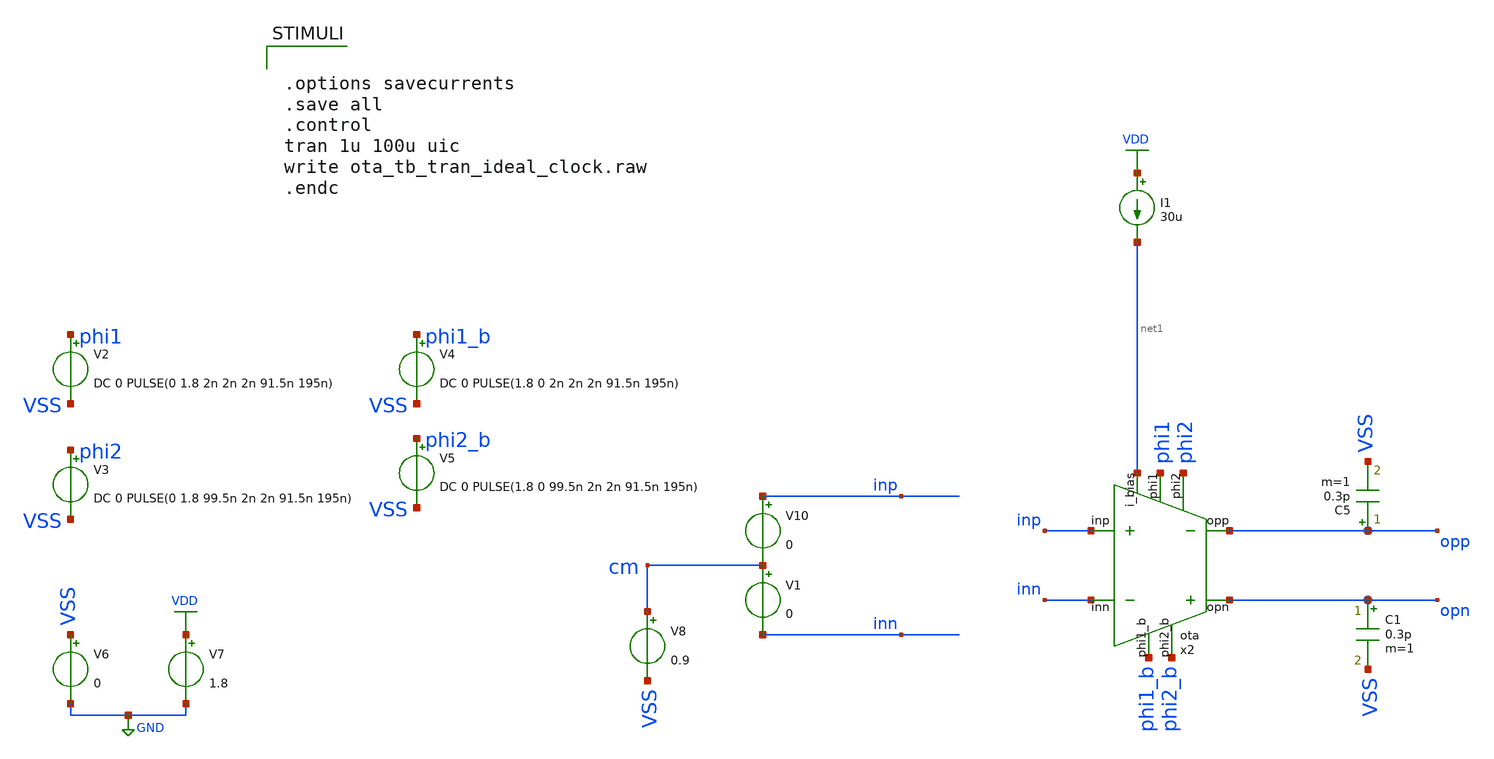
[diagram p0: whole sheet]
** sch_path: verification/schematic_sim/ota_tb_tran_ideal_clock.sch
**.subckt ota_tb_tran_ideal_clock
V6 VSS GND 0
V7 VDD GND 1.8
V8 cm VSS 0.9
V10 inp cm 0
V1 cm inn 0
V2 phi1 VSS DC 0 PULSE(0 1.8 2n 2n 2n 91.5n 195n)
V3 phi2 VSS DC 0 PULSE(0 1.8 99.5n 2n 2n 91.5n 195n)
V4 phi1_b VSS DC 0 PULSE(1.8 0 2n 2n 2n 91.5n 195n)
V5 phi2_b VSS DC 0 PULSE(1.8 0 99.5n 2n 2n 91.5n 195n)
x2 net1 inp inn phi1 phi1_b phi2 phi2_b opp opn 50 350 VDD VSS ota
I1 VDD net1 30u
C5 opp VSS 0.3p m=1
C1 opn VSS 0.3p m=1
**** begin user architecture code

** opencircuitdesign pdks install
.lib /farmshare/home/classes/ee/372/PDKs/open_pdks_1.0.310/sky130/sky130A/libs.tech/ngspice/sky130.lib.spice tt



.options savecurrents
.save all
.control
tran 1u 100u uic
write ota_tb_tran_ideal_clock.raw
.endc


**** end user architecture code
**.ends
.GLOBAL VDD
.GLOBAL GND
.end
